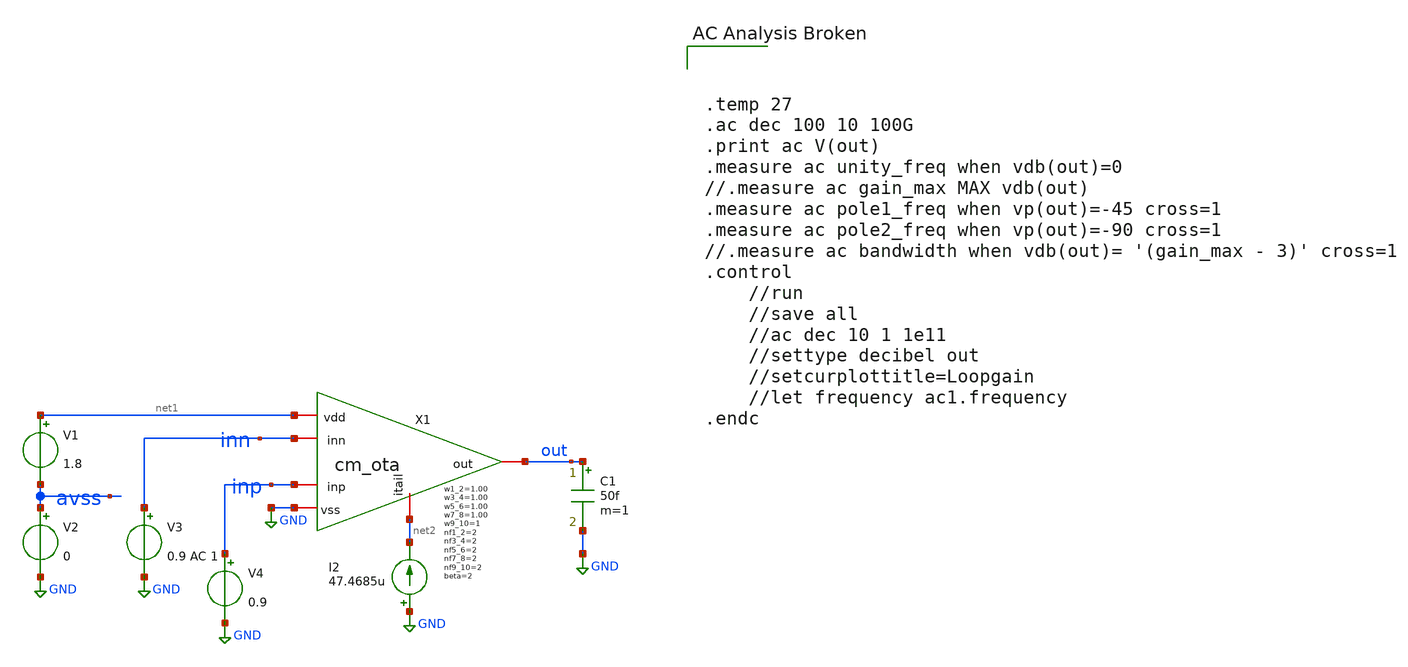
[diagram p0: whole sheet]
** sch_path: ISSCC25/submitted_notebooks/current_mirror_ota_optimization/characterization/sky130/schematics/tb_cm_ota.sch
**.subckt tb_cm_ota
V1 net1 avss 1.8
V2 avss GND 0
C1 out GND 50f m=1
V3 inn GND 0.9 AC 1
V4 inp GND 0.9
X1 net1 out inp inn net2 GND cm_ota w1_2=1.00 w3_4=1.00 w5_6=1.00 w7_8=1.00 w9_10=1 beta=2 nf1_2=2
+ nf3_4=2 nf5_6=2 nf7_8=2 nf9_10=2
I2 GND net2 47.4685u
**** begin user architecture code

** opencircuitdesign pdks isntsall
//.lib /opt/pdk/open_pdks/sky130/sky130A/libs.tech/ngspice/sky130.lib.spice tt





.temp 27
.ac dec 100 10 100G
.print ac V(out)
.measure ac unity_freq when vdb(out)=0
//.measure ac gain_max MAX vdb(out)
.measure ac pole1_freq when vp(out)=-45 cross=1
.measure ac pole2_freq when vp(out)=-90 cross=1
//.measure ac bandwidth when vdb(out)= '(gain_max - 3)' cross=1
.control
	//run
	//save all
	//ac dec 10 1 1e11
	//settype decibel out
	//setcurplottitle=Loopgain
	//let frequency ac1.frequency
.endc





.lib /opt/pdk/open_pdks/sky130/sky130A/libs.tech/ngspice/sky130.lib.spice tt
.temp 27
.option savecurrents
.save all
.ac dec 100 1 100e15
.print ac V(out)
.measure ac gbw when vdb(out)=0
.measure ac dc_gain find vdb(out) at=10
.measure ac pole1_freq when 180*cph(out)/pi=-45 cross=1
.measure ac pole2_freq when 180*cph(out)/pi cross=1
//.measure ac bandwidth when vdb(out)= '(dc_gain - 3)' cross=1
.control
	// run //v1
	// set hcopyscolor=1 //v1
	run
	plot vdb(out) vs frequency
	plot 180*cph(out)/pi vs frequency
	opran 0 0 0 10n 10u 0
	op
	write tb_cm_ota.raw
	echo 'GBWP = ' gbw
	echo 'DC Gain = ' dc_gain
	echo 'pole1 freq = ' pole1_freq
	echo 'pole2 freq = ' pole2_freq
	echo '3dB BW = ' bandwidth
.endc


**** end user architecture code
**.ends

* expanding   symbol:  cm_ota.sym # of pins=6
** sym_path: ISSCC25/submitted_notebooks/current_mirror_ota_optimization/characterization/sky130/schematics/cm_ota.sym
** sch_path: ISSCC25/submitted_notebooks/current_mirror_ota_optimization/characterization/sky130/schematics/cm_ota.sch
.subckt cm_ota vdd out inp inn itail vss  w1_2=1 w3_4=1 w5_6=1 w7_8=1 w9_10=1 beta=2 nf1_2=2 nf3_4=2
+ nf5_6=2 nf7_8=2 nf9_10=2
*.iopin inn
*.iopin inp
*.iopin out
*.iopin vss
*.iopin vdd
*.iopin itail
XM1 ds1_3 inn source source sky130_fd_pr__nfet_01v8 L=0.15 W=w1_2 nf=nf1_2 ad='int((nf+1)/2) * W/nf * 0.29'
+ as='int((nf+2)/2) * W/nf * 0.29' pd='2*int((nf+1)/2) * (W/nf + 0.29)' ps='2*int((nf+2)/2) * (W/nf + 0.29)'
+ nrd='0.29 / W' nrs='0.29 / W' sa=0 sb=0 sd=0 mult=1 m=1
xM3 ds1_3 ds1_3 vdd vdd sky130_fd_pr__pfet_01v8 L=0.15 W=w3_4 nf=nf3_4 ad='int((nf+1)/2) * W/nf * 0.29'
+ as='int((nf+2)/2) * W/nf * 0.29' pd='2*int((nf+1)/2) * (W/nf + 0.29)' ps='2*int((nf+2)/2) * (W/nf + 0.29)'
+ nrd='0.29 / W' nrs='0.29 / W' sa=0 sb=0 sd=0 mult=1 m=1
XM2 ds2_4 inp source source sky130_fd_pr__nfet_01v8 L=0.15 W=w1_2 nf=nf1_2 ad='int((nf+1)/2) * W/nf * 0.29'
+ as='int((nf+2)/2) * W/nf * 0.29' pd='2*int((nf+1)/2) * (W/nf + 0.29)' ps='2*int((nf+2)/2) * (W/nf + 0.29)'
+ nrd='0.29 / W' nrs='0.29 / W' sa=0 sb=0 sd=0 mult=1 m=1
xM4 ds2_4 ds2_4 vdd vdd sky130_fd_pr__pfet_01v8 L=0.15 W=w3_4 nf=nf3_4 ad='int((nf+1)/2) * W/nf * 0.29'
+ as='int((nf+2)/2) * W/nf * 0.29' pd='2*int((nf+1)/2) * (W/nf + 0.29)' ps='2*int((nf+2)/2) * (W/nf + 0.29)'
+ nrd='0.29 / W' nrs='0.29 / W' sa=0 sb=0 sd=0 mult=1 m=1
xM7 ds5_7 ds1_3 vdd vdd sky130_fd_pr__pfet_01v8 L=0.15 W=w7_8 nf=nf7_8 ad='int((nf+1)/2) * W/nf * 0.29'
+ as='int((nf+2)/2) * W/nf * 0.29' pd='2*int((nf+1)/2) * (W/nf + 0.29)' ps='2*int((nf+2)/2) * (W/nf + 0.29)'
+ nrd='0.29 / W' nrs='0.29 / W' sa=0 sb=0 sd=0 mult=1 m=1
XM5 ds5_7 ds5_7 vss vss sky130_fd_pr__nfet_01v8 L=0.15 W=w5_6 nf=nf5_6 ad='int((nf+1)/2) * W/nf * 0.29'
+ as='int((nf+2)/2) * W/nf * 0.29' pd='2*int((nf+1)/2) * (W/nf + 0.29)' ps='2*int((nf+2)/2) * (W/nf + 0.29)'
+ nrd='0.29 / W' nrs='0.29 / W' sa=0 sb=0 sd=0 mult=1 m=1
XM6 out ds5_7 vss vss sky130_fd_pr__nfet_01v8 L=0.15 W=w5_6 nf=nf5_6 ad='int((nf+1)/2) * W/nf * 0.29'
+ as='int((nf+2)/2) * W/nf * 0.29' pd='2*int((nf+1)/2) * (W/nf + 0.29)' ps='2*int((nf+2)/2) * (W/nf + 0.29)'
+ nrd='0.29 / W' nrs='0.29 / W' sa=0 sb=0 sd=0 mult=1 m=1
xM8 out ds2_4 vdd vdd sky130_fd_pr__pfet_01v8 L=0.15 W=w7_8 nf=nf7_8 ad='int((nf+1)/2) * W/nf * 0.29'
+ as='int((nf+2)/2) * W/nf * 0.29' pd='2*int((nf+1)/2) * (W/nf + 0.29)' ps='2*int((nf+2)/2) * (W/nf + 0.29)'
+ nrd='0.29 / W' nrs='0.29 / W' sa=0 sb=0 sd=0 mult=1 m=1
XM9 source itail vss vss sky130_fd_pr__nfet_01v8 L=0.15 W=w9_10 nf=nf9_10 ad='int((nf+1)/2) * W/nf * 0.29'
+ as='int((nf+2)/2) * W/nf * 0.29' pd='2*int((nf+1)/2) * (W/nf + 0.29)' ps='2*int((nf+2)/2) * (W/nf + 0.29)'
+ nrd='0.29 / W' nrs='0.29 / W' sa=0 sb=0 sd=0 mult=1 m=1
XM10 itail itail vss vss sky130_fd_pr__nfet_01v8 L=0.15 W=w9_10 nf=nf1_2 ad='int((nf+1)/2) * W/nf * 0.29'
+ as='int((nf+2)/2) * W/nf * 0.29' pd='2*int((nf+1)/2) * (W/nf + 0.29)' ps='2*int((nf+2)/2) * (W/nf + 0.29)'
+ nrd='0.29 / W' nrs='0.29 / W' sa=0 sb=0 sd=0 mult=1 m=1
.ends

.GLOBAL GND
.end
